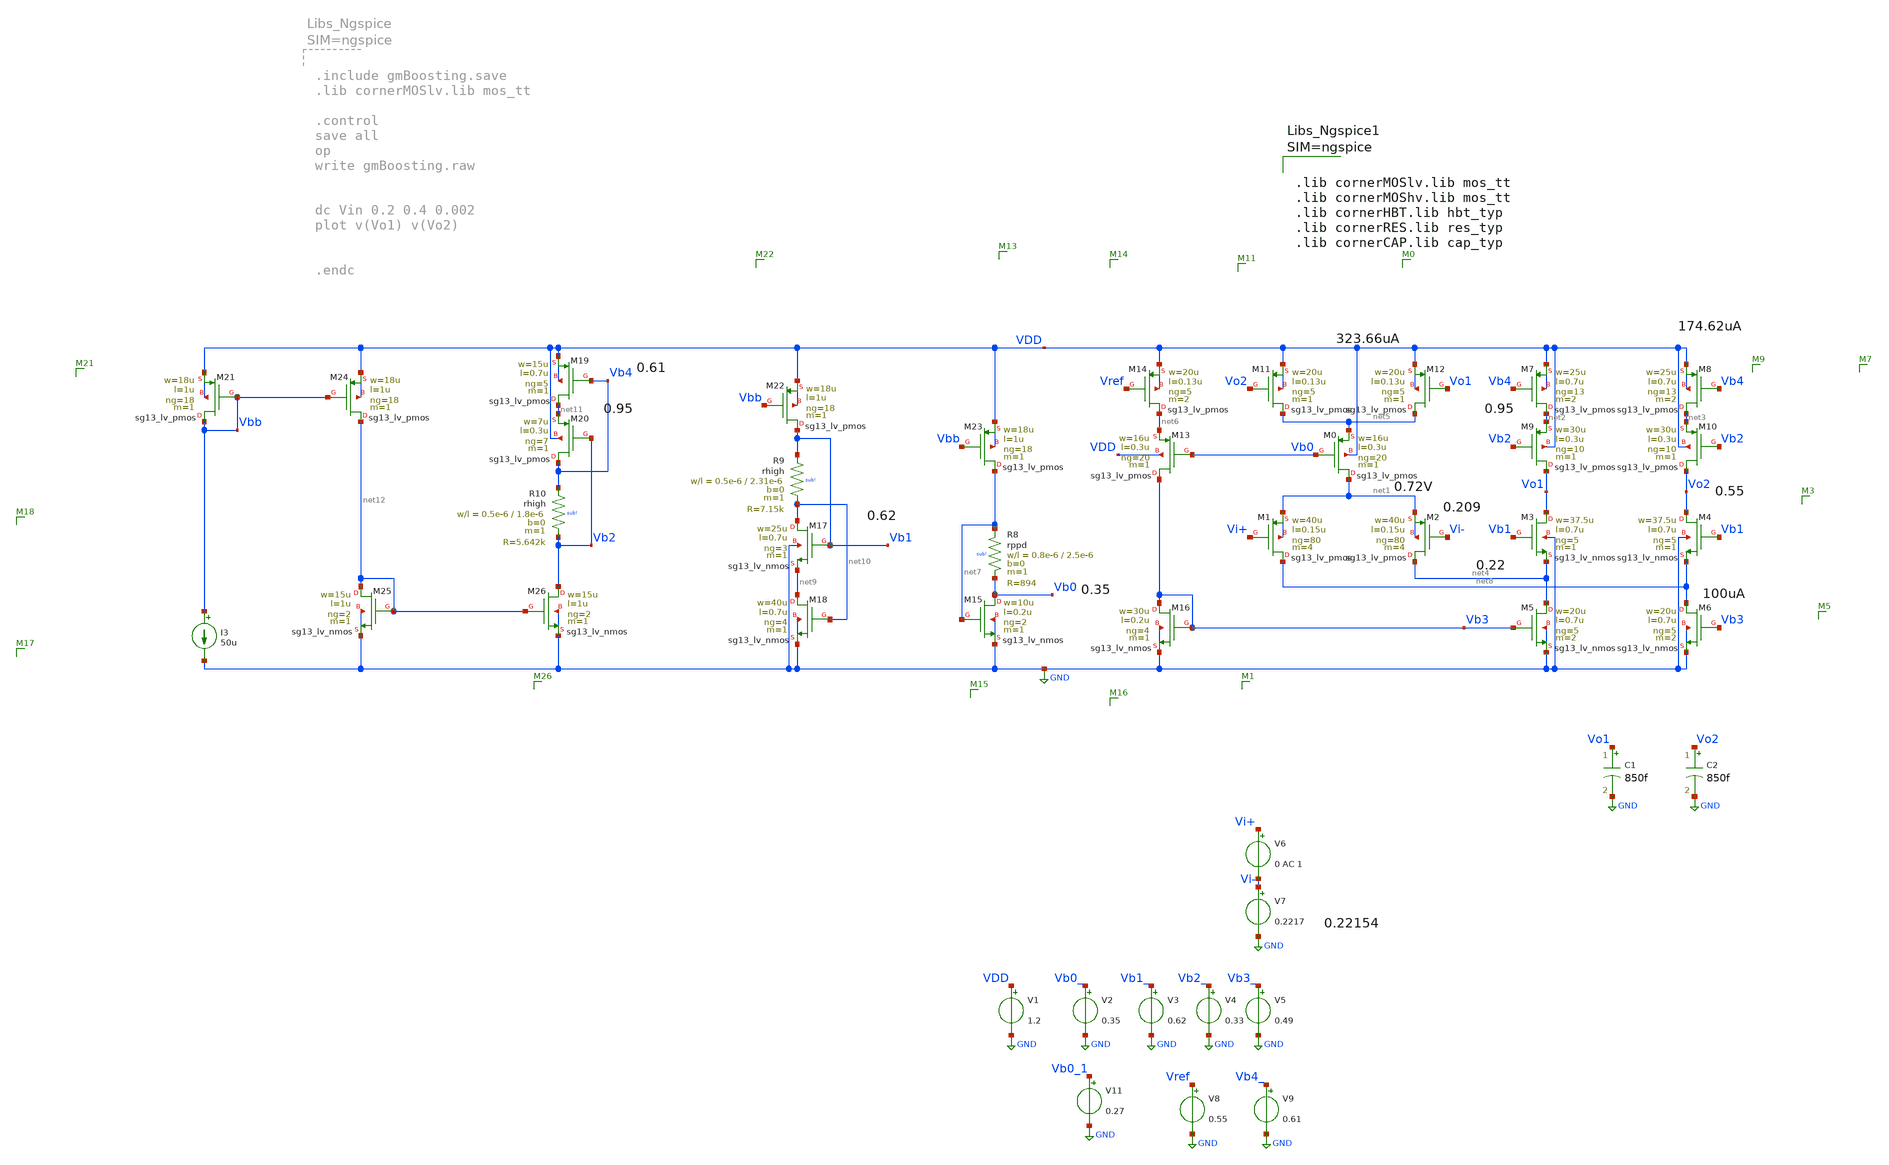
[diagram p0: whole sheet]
** sch_path: sch/testing/gmBoosting.sch
**.subckt gmBoosting
XM7 net2 Vb4 VDD VDD sg13_lv_pmos w=25u l=0.7u ng=13 m=2 mm_ok=1
XM1 net8 Vi+ net1 net1 sg13_lv_pmos w=40u l=0.15u ng=80 m=4 mm_ok=1
XM2 net4 Vi- net1 net1 sg13_lv_pmos w=40u l=0.15u ng=80 m=4 mm_ok=1
XM0 net1 Vb0 net5 VDD sg13_lv_pmos w=16u l=0.3u ng=20 m=1 mm_ok=1
XM6 net8 Vb3 GND GND sg13_lv_nmos w=20u l=0.7u ng=5 m=2 mm_ok=1
V1 VDD GND 1.2
V2 Vb0_ GND 0.35
V3 Vb1_ GND 0.62
V4 Vb2_ GND 0.33
V5 Vb3_ GND 0.49
V7 Vi- GND 0.2217
V6 Vi+ Vi- 0 AC 1
C1 Vo1 GND 850f m=1
C2 Vo2 GND 850f m=1
XM9 Vo1 Vb2 net2 VDD sg13_lv_pmos w=30u l=0.3u ng=10 m=1 mm_ok=1
XM10 Vo2 Vb2 net3 VDD sg13_lv_pmos w=30u l=0.3u ng=10 m=1 mm_ok=1
V9 Vb4_ GND 0.61
XM8 net3 Vb4 VDD VDD sg13_lv_pmos w=25u l=0.7u ng=13 m=2 mm_ok=1
V11 Vb0_1 GND 0.27
XM11 net5 Vo2 VDD VDD sg13_lv_pmos w=20u l=0.13u ng=5 m=1 mm_ok=1
XM12 net5 Vo1 VDD VDD sg13_lv_pmos w=20u l=0.13u ng=5 m=1 mm_ok=1
XM14 net6 Vref VDD VDD sg13_lv_pmos w=20u l=0.13u ng=5 m=2 mm_ok=1
V8 Vref GND 0.55
XM15 Vb0 net7 GND GND sg13_lv_nmos w=10u l=0.2u ng=2 m=1 mm_ok=1
XM16 Vb3 Vb3 GND GND sg13_lv_nmos w=30u l=0.2u ng=4 m=1 mm_ok=1
XR8 net7 Vb0 sub! rppd w=0.8e-6 l=2.5e-6 m=1 b=0 mm_ok=1
XM13 Vb3 Vb0 net6 VDD sg13_lv_pmos w=16u l=0.3u ng=20 m=1 mm_ok=1
XM5 net4 Vb3 GND GND sg13_lv_nmos w=20u l=0.7u ng=5 m=2 mm_ok=1
XM3 Vo1 Vb1 net4 GND sg13_lv_nmos w=37.5u l=0.7u ng=5 m=1 mm_ok=1
XM4 Vo2 Vb1 net8 GND sg13_lv_nmos w=37.5u l=0.7u ng=5 m=1 mm_ok=1
XR9 Vb1 net10 sub! rhigh w=0.5e-6 l=2.31e-6 m=1 b=0 mm_ok=1
XM17 net10 Vb1 net9 GND sg13_lv_nmos w=25u l=0.7u ng=3 m=1 mm_ok=1
XM18 net9 net10 GND GND sg13_lv_nmos w=40u l=0.7u ng=4 m=1 mm_ok=1
XM19 net11 Vb4 VDD VDD sg13_lv_pmos w=15u l=0.7u ng=5 m=1 mm_ok=1
XM20 Vb4 Vb2 net11 VDD sg13_lv_pmos w=7u l=0.3u ng=7 m=1 mm_ok=1
XR10 Vb4 Vb2 sub! rhigh w=0.5e-6 l=1.8e-6 m=1 b=0 mm_ok=1
I3 Vbb GND 50u
XM21 Vbb Vbb VDD VDD sg13_lv_pmos w=18u l=1u ng=18 m=1 mm_ok=1
XM22 Vb1 Vbb VDD VDD sg13_lv_pmos w=18u l=1u ng=18 m=1 mm_ok=1
XM23 net7 Vbb VDD VDD sg13_lv_pmos w=18u l=1u ng=18 m=1 mm_ok=1
XM24 net12 Vbb VDD VDD sg13_lv_pmos w=18u l=1u ng=18 m=1 mm_ok=1
XM25 net12 net12 GND GND sg13_lv_nmos w=15u l=1u ng=2 m=1 mm_ok=1
XM26 Vb2 net12 GND GND sg13_lv_nmos w=15u l=1u ng=2 m=1 mm_ok=1
**** begin user architecture code



.lib cornerMOSlv.lib mos_tt
.lib cornerMOShv.lib mos_tt
.lib cornerHBT.lib hbt_typ
.lib cornerRES.lib res_typ
.lib cornerCAP.lib cap_typ






.include gmBoosting.save
.lib cornerMOSlv.lib mos_tt
.temp 65
.control
save all
op
write gmBoosting.raw


ac dec 1k 1 10G
let Av = db((v(Vo1)-v(Vo2)))
meas ac UGBW WHEN Av=0
let phase_vec = 180/pi*cph(v(Vo1)-v(Vo2))

meas ac phase FIND phase_vec WHEN frequency=UGBW
let PM = phase+180
print PM

plot Av
plot phase_vec



.endc



**** end user architecture code
**.ends
.GLOBAL GND
.end
